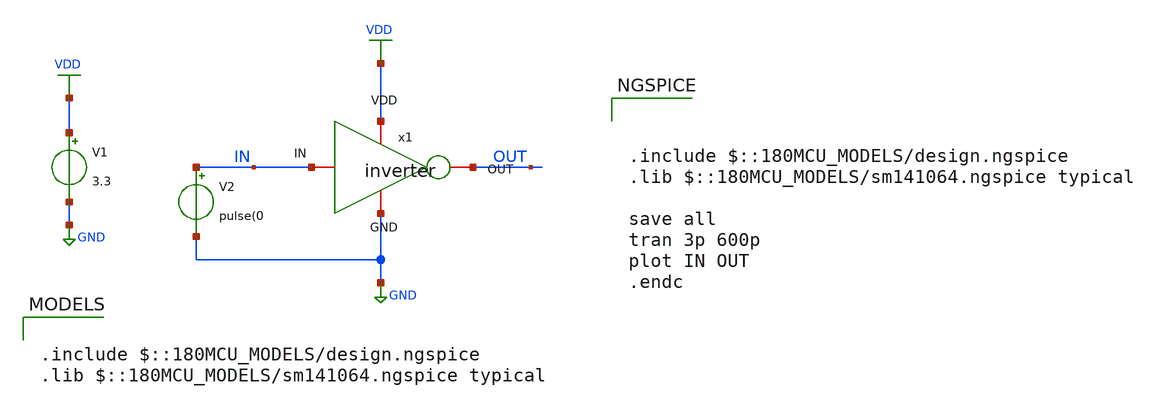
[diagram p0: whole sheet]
** sch_path: ipdesignguide/tutorial/inverter/inverter_tb.sch
**.subckt inverter_tb
V1 VDD GND 3.3
V2 IN GND pulse(0
x1 VDD OUT IN GND inverter
**** begin user architecture code


.include $::180MCU_MODELS/design.ngspice
.lib $::180MCU_MODELS/sm141064.ngspice typical





.include $::180MCU_MODELS/design.ngspice
.lib $::180MCU_MODELS/sm141064.ngspice typical

save all
tran 3p 600p
plot IN OUT
.endc


**** end user architecture code
**.ends

* expanding   symbol:
*+  /work/stu/hzhang/project/OpenXRAM/ipdesignguide/tutorial/inverter/inverter.sym # of pins=4
** sym_path: ipdesignguide/tutorial/inverter/inverter.sym
** sch_path: ipdesignguide/tutorial/inverter/inverter.sch
.subckt inverter VDD OUT IN GND
*.iopin OUT
*.iopin VDD
*.iopin GND
*.iopin IN
XM1 OUT IN GND GND nmos_3p3 L=0.28u W=0.22u nf=1 ad='int((nf+1)/2) * W/nf * 0.18u' as='int((nf+2)/2) * W/nf * 0.18u'
+ pd='2*int((nf+1)/2) * (W/nf + 0.18u)' ps='2*int((nf+2)/2) * (W/nf + 0.18u)' nrd='0.18u / W' nrs='0.18u / W'
+ sa=0 sb=0 sd=0 m=1
XM2 OUT IN VDD VDD pmos_3p3 L=0.28u W=0.44u nf=1 ad='int((nf+1)/2) * W/nf * 0.18u' as='int((nf+2)/2) * W/nf * 0.18u'
+ pd='2*int((nf+1)/2) * (W/nf + 0.18u)' ps='2*int((nf+2)/2) * (W/nf + 0.18u)' nrd='0.18u / W' nrs='0.18u / W'
+ sa=0 sb=0 sd=0 m=1
.ends

.GLOBAL VDD
.GLOBAL GND
.end
